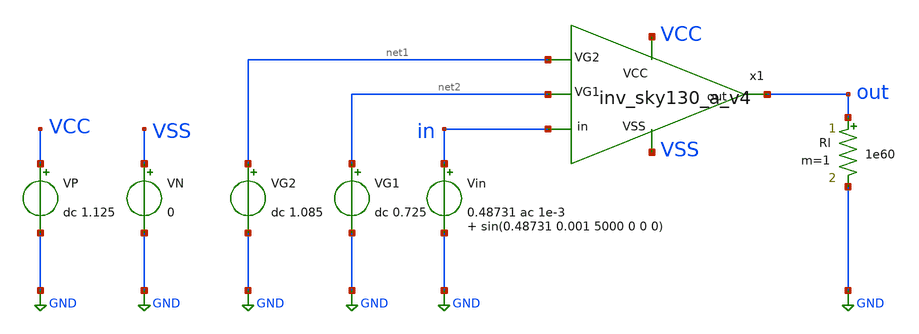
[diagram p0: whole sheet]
** sch_path: Amplifier_Inv/xschem/v4/tb_inv_sky130_a_v4.sch
**.subckt tb_inv_sky130_a_v4
VN VSS GND 0
VP VCC GND dc 1.125
.save i(vp)
Vin in GND 0.48731 ac 1e-3 sin(0.48731 0.001 5000 0 0 0)
.save i(vin)
Rl out GND 1e60 m=1
VG2 net1 GND dc 1.085
VG1 net2 GND dc 0.725
x1 net2 VCC net1 out in VSS inv_sky130_a_v4
**** begin user architecture code

** opencircuitdesign pdks install
.lib $::SKYWATER_MODELS/sky130.lib.spice ss



.control

  op
  save all
  let gmn = @m.x1.xm4.msky130_fd_pr__nfet_01v8[gm]
  let gmp = @m.x1.xm5'.msky130_fd_pr__pfet_01v8[gm]
  let gdsn = @m.x1.xm4.msky130_fd_pr__nfet_01v8[gds]
  let gdsp = @m.x1.xm5.msky130_fd_pr__pfet_01v8[gds]
  let cgsn = @m.x1.xm4.msky130_fd_pr__nfet_01v8[cgs]
  let cgsp = @m.x1.xm5.msky130_fd_pr__pfet_01v8[cgs]
  let cgdn = @m.x1.xm4.msky130_fd_pr__nfet_01v8[cgd]
  let cgdp = @m.x1.xm5.msky130_fd_pr__pfet_01v8[cgd]
  write tb_inv_sky130_a_op_v4.raw gmn gmp gdsn gdsp cgsn cgsp cgdn cgdp

  ac dec 1000 1 1e8
  save all
  let gain = db(v(out)/v(in))
  let gain_vs1 = db(v(x1.vs1)/v(in))
  let phase = phase(v(out)/v(in))
  write tb_inv_sky130_a_AC_v4.raw gain gain_vs1

  noise v(out) Vin dec 1000 300 10k 10
  save all
  write tb_inv_sky130_a_noise_v4.raw

  noise v(out) Vin dec 1000 300 10k
  save all
  setplot noise1
  write tb_inv_sky130_a_noise_spectrum_v4.raw

  dc Vin 0 1.125 0.00001
  save all v(out) v(x1.vs1) v(x1.vd1)
  write tb_inv_sky130_a_DC_v4.raw v(out) v(x1.vs1) v(x1.vd1)

  tran 0.1u 4m
  save all
  let pw_in = i(Vin)*v(in)
  let pw_vcc = i(Vp)*1.125
  let pw_vg1 = i(Vg1)*0.725
  let pw_vg2 = i(Vg2)*1.085
  let pw_total = pw_in+pw_vcc
  meas tran avg_pw_total AVG pw_total FROM=0 TO=2m
  meas tran avg_pw_in AVG pw_in FROM=0 TO=2m
  meas tran avg_pw_vcc AVG pw_vcc FROM=0 TO=2m
  write tb_inv_sky130_a_tran_v4.raw v(in) v(out) avg_pw_total

.endc


**** end user architecture code
**.ends

* expanding   symbol:  v4/inv_sky130_a_v4.sym # of pins=6
** sym_path: Amplifier_Inv/xschem/v4/inv_sky130_a_v4.sym
** sch_path: Amplifier_Inv/xschem/v4/inv_sky130_a_v4.sch
.subckt inv_sky130_a_v4 VG1 VCC VG2 out in VSS
*.ipin in
*.opin out
*.ipin VG1
*.ipin VG2
*.ipin VSS
*.ipin VCC
XC1 in VD1 sky130_fd_pr__cap_mim_m3_1 W=26 L=26 MF=1 m=1
XM4 VS1 VD1 VSS VSS sky130_fd_pr__nfet_01v8 L=1 W=250 nf=10 ad='int((10 + 1)/2) * 250 / 10 * 0.29' as='int((10
+ + 2)/2) * 250 / 10 * 0.29' pd='2*int((10 + 1)/2) * (250 / 10 + 0.29)' ps='2*int((10 + 2)/2) * (250 /
+ 10 + 0.29)' nrd='0.29 / 250 ' nrs='0.29 / 250 ' sa=0 sb=0 sd=0 mult=1 m=1
XM5 VS1 VD1 VCC VCC sky130_fd_pr__pfet_01v8 L=0.25 W=200 nf=8 ad='int((nf+1)/2) * W/nf * 0.29' as='int((nf+2)/2)
+ * W/nf * 0.29' pd='2*int((nf+1)/2) * (W/nf + 0.29)' ps='2*int((nf+2)/2) * (W/nf + 0.29)' nrd='0.29 /
+ W' nrs='0.29 / W' sa=0 sb=0 sd=0 mult=1 m=1
XM2 VS1 VG2 out VSS sky130_fd_pr__nfet_01v8 L=0.15 W=0.5 nf=1 ad='int((1 + 1)/2) * 0.5 / 1 * 0.29' as='int((1
+ + 2)/2) * 0.5 / 1 * 0.29' pd='2*int((1 + 1)/2) * (0.5 / 1 + 0.29)' ps='2*int((1 + 2)/2) * (0.5 / 1 +
+ 0.29)' nrd='0.29 / 0.5 ' nrs='0.29 / 0.5 ' sa=0 sb=0 sd=0 mult=1 m=1
XM3 VSS out VSS VSS sky130_fd_pr__nfet_01v8 L=10 W=100 nf=4 ad='int((4 + 1)/2) * 100 / 4 * 0.29' as='int((4
+ + 2)/2) * 100 / 4 * 0.29' pd='2*int((4 + 1)/2) * (100 / 4 + 0.29)' ps='2*int((4 + 2)/2) * (100 / 4 +
+ 0.29)' nrd='0.29 / 100 ' nrs='0.29 / 100 ' sa=0 sb=0 sd=0 mult=1 m=1
XM1 VD1 VG1 VS1 VSS sky130_fd_pr__nfet_01v8 L=0.15 W=0.5 nf=1 ad='int((1 + 1)/2) * 0.5 / 1 * 0.29' as='int((1
+ + 2)/2) * 0.5 / 1 * 0.29' pd='2*int((1 + 1)/2) * (0.5 / 1 + 0.29)' ps='2*int((1 + 2)/2) * (0.5 / 1 +
+ 0.29)' nrd='0.29 / 0.5 ' nrs='0.29 / 0.5 ' sa=0 sb=0 sd=0 mult=1 m=1
.ends

.GLOBAL GND
.end
